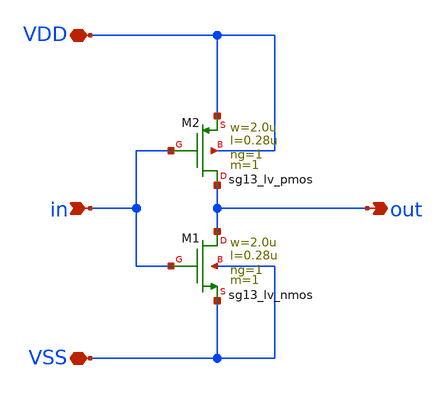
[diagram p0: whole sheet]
** sch_path: blocks/composite/dpi_adexp_neuron/design_data/xschem/dev/inv.sch
**.subckt inv VDD in VSS out
*.iopin VDD
*.ipin in
*.iopin VSS
*.opin out
XM1 out in VSS VSS sg13_lv_nmos w=2.0u l=0.28u ng=1 m=1 mm_ok=1
XM2 out in VDD VDD sg13_lv_pmos w=2.0u l=0.28u ng=1 m=1 mm_ok=1
**.ends
.end
